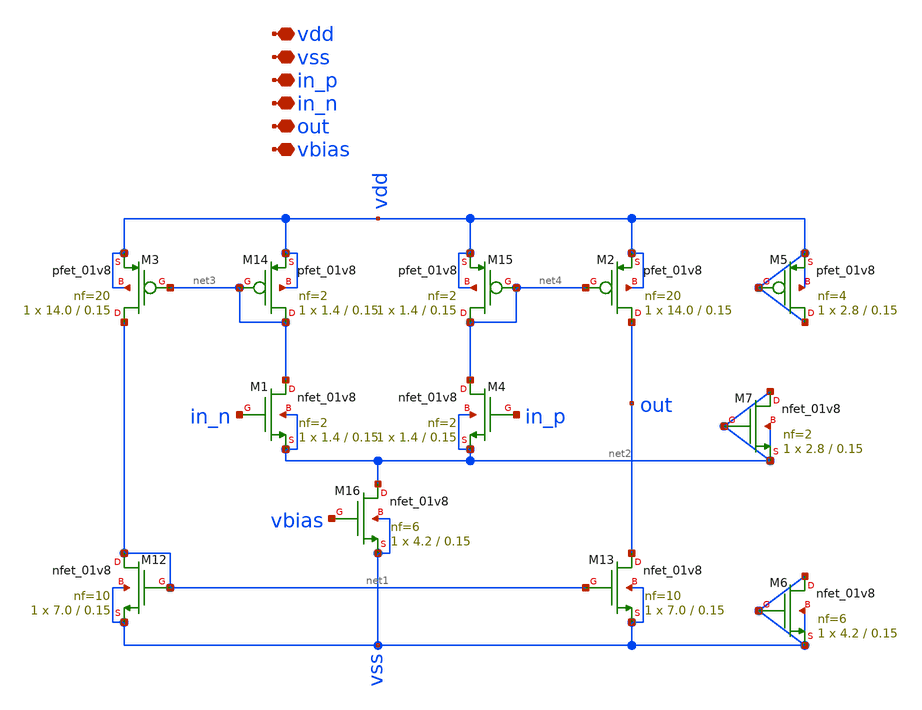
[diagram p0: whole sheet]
** sch_path: xschem/ota_2.sch
**.subckt ota_2 vdd vss in_p in_n out vbias
*.iopin vdd
*.iopin vss
*.iopin in_p
*.iopin in_n
*.iopin out
*.iopin vbias
XM1 net3 in_n net2 net2 sky130_fd_pr__nfet_01v8 L=0.15 W=1.4 nf=2 ad='int((nf+1)/2) * W/nf * 0.29' as='int((nf+2)/2) * W/nf * 0.29'
+ pd='2*int((nf+1)/2) * (W/nf + 0.29)' ps='2*int((nf+2)/2) * (W/nf + 0.29)' nrd='0.29 / W' nrs='0.29 / W'
+ sa=0 sb=0 sd=0 mult=1 m=1
XM3 net1 net3 vdd vdd sky130_fd_pr__pfet_01v8 L=0.15 W=14.0 nf=20 ad='int((nf+1)/2) * W/nf * 0.29' as='int((nf+2)/2) * W/nf * 0.29'
+ pd='2*int((nf+1)/2) * (W/nf + 0.29)' ps='2*int((nf+2)/2) * (W/nf + 0.29)' nrd='0.29 / W' nrs='0.29 / W'
+ sa=0 sb=0 sd=0 mult=1 m=1
XM2 out net4 vdd vdd sky130_fd_pr__pfet_01v8 L=0.15 W=14.0 nf=20 ad='int((nf+1)/2) * W/nf * 0.29' as='int((nf+2)/2) * W/nf * 0.29'
+ pd='2*int((nf+1)/2) * (W/nf + 0.29)' ps='2*int((nf+2)/2) * (W/nf + 0.29)' nrd='0.29 / W' nrs='0.29 / W'
+ sa=0 sb=0 sd=0 mult=1 m=1
XM4 net4 in_p net2 net2 sky130_fd_pr__nfet_01v8 L=0.15 W=1.4 nf=2 ad='int((nf+1)/2) * W/nf * 0.29' as='int((nf+2)/2) * W/nf * 0.29'
+ pd='2*int((nf+1)/2) * (W/nf + 0.29)' ps='2*int((nf+2)/2) * (W/nf + 0.29)' nrd='0.29 / W' nrs='0.29 / W'
+ sa=0 sb=0 sd=0 mult=1 m=1
XM12 net1 net1 vss vss sky130_fd_pr__nfet_01v8 L=0.15 W=7.0 nf=10 ad='int((nf+1)/2) * W/nf * 0.29' as='int((nf+2)/2) * W/nf * 0.29'
+ pd='2*int((nf+1)/2) * (W/nf + 0.29)' ps='2*int((nf+2)/2) * (W/nf + 0.29)' nrd='0.29 / W' nrs='0.29 / W'
+ sa=0 sb=0 sd=0 mult=1 m=1
XM13 out net1 vss vss sky130_fd_pr__nfet_01v8 L=0.15 W=7.0 nf=10 ad='int((nf+1)/2) * W/nf * 0.29' as='int((nf+2)/2) * W/nf * 0.29'
+ pd='2*int((nf+1)/2) * (W/nf + 0.29)' ps='2*int((nf+2)/2) * (W/nf + 0.29)' nrd='0.29 / W' nrs='0.29 / W'
+ sa=0 sb=0 sd=0 mult=1 m=1
XM14 net3 net3 vdd vdd sky130_fd_pr__pfet_01v8 L=0.15 W=1.4 nf=2 ad='int((nf+1)/2) * W/nf * 0.29' as='int((nf+2)/2) * W/nf * 0.29'
+ pd='2*int((nf+1)/2) * (W/nf + 0.29)' ps='2*int((nf+2)/2) * (W/nf + 0.29)' nrd='0.29 / W' nrs='0.29 / W'
+ sa=0 sb=0 sd=0 mult=1 m=1
XM15 net4 net4 vdd vdd sky130_fd_pr__pfet_01v8 L=0.15 W=1.4 nf=2 ad='int((nf+1)/2) * W/nf * 0.29' as='int((nf+2)/2) * W/nf * 0.29'
+ pd='2*int((nf+1)/2) * (W/nf + 0.29)' ps='2*int((nf+2)/2) * (W/nf + 0.29)' nrd='0.29 / W' nrs='0.29 / W'
+ sa=0 sb=0 sd=0 mult=1 m=1
XM16 net2 vbias vss vss sky130_fd_pr__nfet_01v8 L=0.15 W=4.2 nf=6 ad='int((nf+1)/2) * W/nf * 0.29' as='int((nf+2)/2) * W/nf * 0.29'
+ pd='2*int((nf+1)/2) * (W/nf + 0.29)' ps='2*int((nf+2)/2) * (W/nf + 0.29)' nrd='0.29 / W' nrs='0.29 / W'
+ sa=0 sb=0 sd=0 mult=1 m=1
XM5 vdd vdd vdd vdd sky130_fd_pr__pfet_01v8 L=0.15 W=2.8 nf=4 ad='int((nf+1)/2) * W/nf * 0.29' as='int((nf+2)/2) * W/nf * 0.29'
+ pd='2*int((nf+1)/2) * (W/nf + 0.29)' ps='2*int((nf+2)/2) * (W/nf + 0.29)' nrd='0.29 / W' nrs='0.29 / W'
+ sa=0 sb=0 sd=0 mult=1 m=1
XM6 vss vss vss vss sky130_fd_pr__nfet_01v8 L=0.15 W=4.2 nf=6 ad='int((nf+1)/2) * W/nf * 0.29' as='int((nf+2)/2) * W/nf * 0.29'
+ pd='2*int((nf+1)/2) * (W/nf + 0.29)' ps='2*int((nf+2)/2) * (W/nf + 0.29)' nrd='0.29 / W' nrs='0.29 / W'
+ sa=0 sb=0 sd=0 mult=1 m=1
XM7 net2 net2 net2 net2 sky130_fd_pr__nfet_01v8 L=0.15 W=2.8 nf=2 ad='int((nf+1)/2) * W/nf * 0.29' as='int((nf+2)/2) * W/nf * 0.29'
+ pd='2*int((nf+1)/2) * (W/nf + 0.29)' ps='2*int((nf+2)/2) * (W/nf + 0.29)' nrd='0.29 / W' nrs='0.29 / W'
+ sa=0 sb=0 sd=0 mult=1 m=1
**.ends
.end
